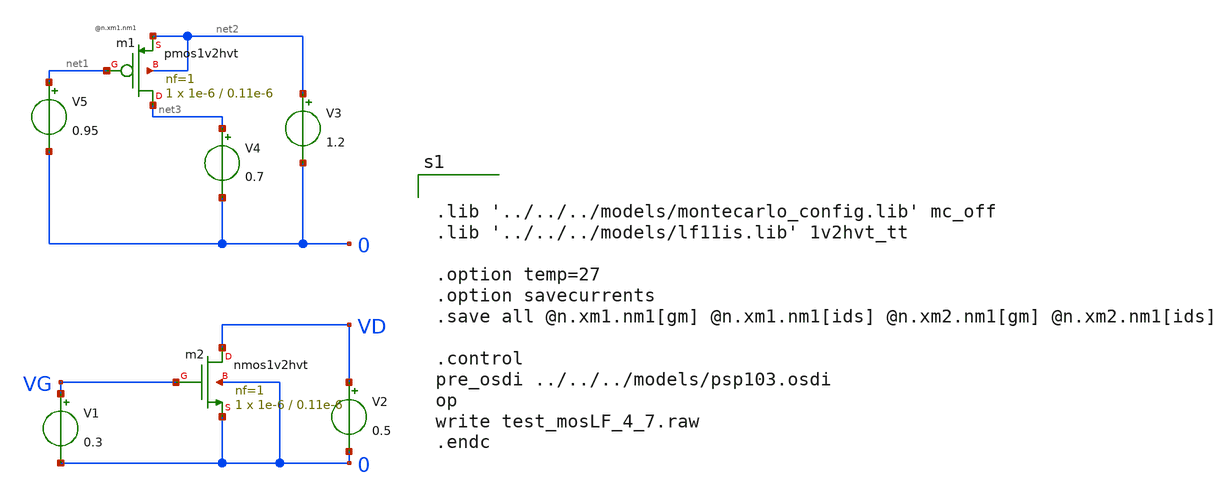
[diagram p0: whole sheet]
** sch_path: test_mosLF_4_7.sch
**.subckt test_mosLF_4_7
V1 VG 0 0.3
V2 VD 0 0.5
V3 net2 0 1.2
V4 net3 0 0.7
V5 net1 0 0.95
xm1 net3 net1 net2 net2 pmos1v2hvt L=0.11e-6 W=1e-6 nf=1 abdrain='int((nf+1)/2) * W/nf * 0.30e-6' absource='int((nf+2)/2) * W/nf * 0.30e-6'
+ lsdrain='2*int((nf+1)/2) * (W/nf + 0.30e-6)' lssource='2*int((nf+2)/2) * (W/nf + 0.30e-6)' dta=0 nrd='0.30e-6 / W'
+ nrs='0.30e-6 / W' sa=0.36e-6 sb=0.36e-6 sd=0 mult=1 m=1
xm2 VD VG 0 0 nmos1v2hvt L=0.11e-6 W=1e-6 nf=1 abdrain='int((nf+1)/2) * W/nf * 0.30e-6' absource='int((nf+2)/2) * W/nf * 0.30e-6'
+ lsdrain='2*int((nf+1)/2) * (W/nf + 0.30e-6)' lssource='2*int((nf+2)/2) * (W/nf + 0.30e-6)' dta=0 nrd='0.30e-6 / W'
+ nrs='0.30e-6 / W' sa=0.36e-6 sb=0.36e-6 sd=0 mult=1 m=1
**** begin user architecture code


.lib '../../../models/montecarlo_config.lib' mc_off
.lib '../../../models/lf11is.lib' 1v2hvt_tt

.option temp=27
.option savecurrents
.save all @n.xm1.nm1[gm] @n.xm1.nm1[ids] @n.xm2.nm1[gm] @n.xm2.nm1[ids]

.control
pre_osdi ../../../models/psp103.osdi
op
write test_mosLF_4_7.raw
.endc


**** end user architecture code
**.ends
.end
